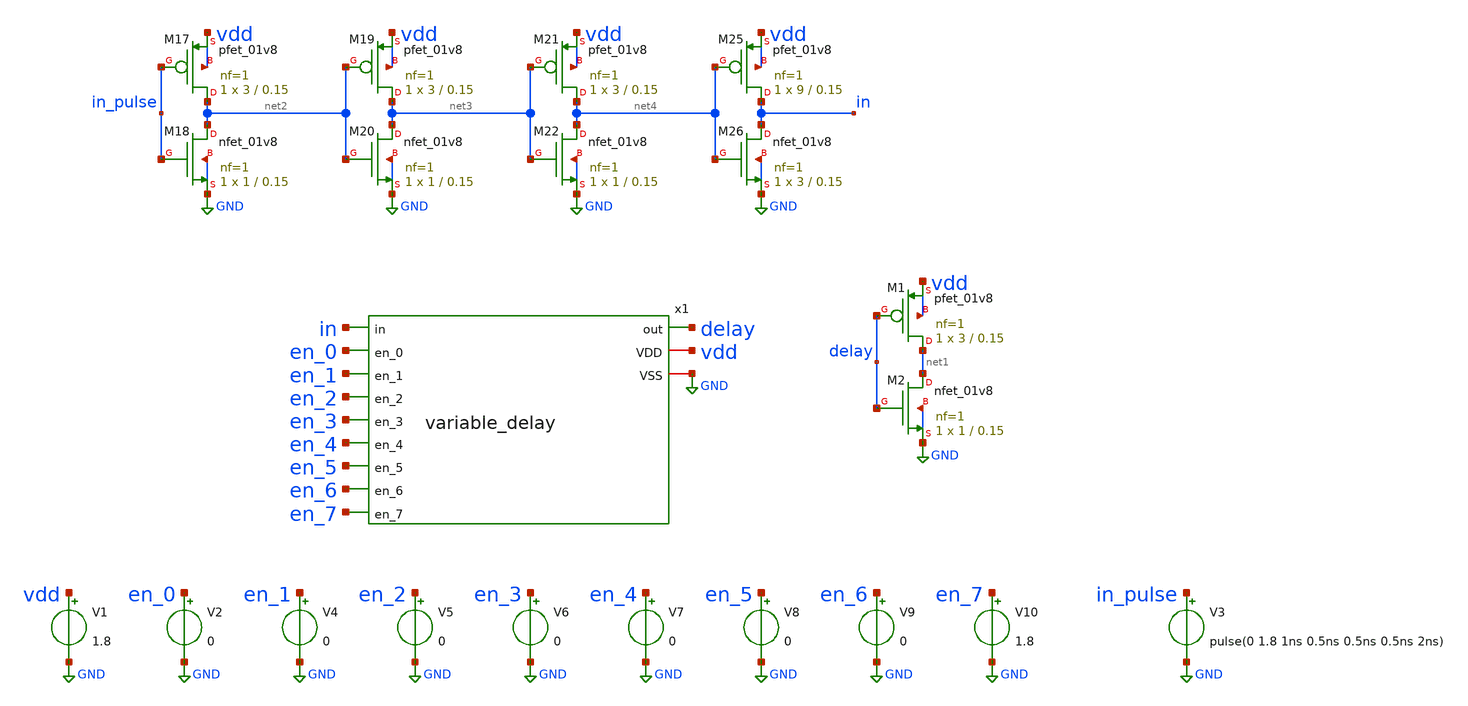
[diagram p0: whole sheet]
** sch_path: xschem/variable_delay_tb.sch
**.subckt variable_delay_tb
x1 in en_0 en_1 en_2 en_3 en_4 en_5 en_6 en_7 delay vdd GND variable_delay
V1 vdd GND 1.8
V3 in_pulse GND pulse(0 1.8 1ns 0.5ns 0.5ns 0.5ns 2ns)
XM1 net1 delay vdd vdd sky130_fd_pr__pfet_01v8 L=0.15 W=3 nf=1 ad='int((nf+1)/2) * W/nf * 0.29' as='int((nf+2)/2) * W/nf * 0.29'
+ pd='2*int((nf+1)/2) * (W/nf + 0.29)' ps='2*int((nf+2)/2) * (W/nf + 0.29)' nrd='0.29 / W' nrs='0.29 / W'
+ sa=0 sb=0 sd=0 mult=1 m=1
XM2 net1 delay GND GND sky130_fd_pr__nfet_01v8 L=0.15 W=1 nf=1 ad='int((nf+1)/2) * W/nf * 0.29' as='int((nf+2)/2) * W/nf * 0.29'
+ pd='2*int((nf+1)/2) * (W/nf + 0.29)' ps='2*int((nf+2)/2) * (W/nf + 0.29)' nrd='0.29 / W' nrs='0.29 / W'
+ sa=0 sb=0 sd=0 mult=1 m=1
V2 en_0 GND 0
V4 en_1 GND 0
V5 en_2 GND 0
V6 en_3 GND 0
V7 en_4 GND 0
V8 en_5 GND 0
V9 en_6 GND 0
V10 en_7 GND 1.8
XM17 net2 in_pulse vdd vdd sky130_fd_pr__pfet_01v8 L=0.15 W=3 nf=1 ad='int((nf+1)/2) * W/nf * 0.29' as='int((nf+2)/2) * W/nf * 0.29'
+ pd='2*int((nf+1)/2) * (W/nf + 0.29)' ps='2*int((nf+2)/2) * (W/nf + 0.29)' nrd='0.29 / W' nrs='0.29 / W'
+ sa=0 sb=0 sd=0 mult=1 m=1
XM18 net2 in_pulse GND GND sky130_fd_pr__nfet_01v8 L=0.15 W=1 nf=1 ad='int((nf+1)/2) * W/nf * 0.29' as='int((nf+2)/2) * W/nf * 0.29'
+ pd='2*int((nf+1)/2) * (W/nf + 0.29)' ps='2*int((nf+2)/2) * (W/nf + 0.29)' nrd='0.29 / W' nrs='0.29 / W'
+ sa=0 sb=0 sd=0 mult=1 m=1
XM19 net3 net2 vdd vdd sky130_fd_pr__pfet_01v8 L=0.15 W=3 nf=1 ad='int((nf+1)/2) * W/nf * 0.29' as='int((nf+2)/2) * W/nf * 0.29'
+ pd='2*int((nf+1)/2) * (W/nf + 0.29)' ps='2*int((nf+2)/2) * (W/nf + 0.29)' nrd='0.29 / W' nrs='0.29 / W'
+ sa=0 sb=0 sd=0 mult=1 m=1
XM20 net3 net2 GND GND sky130_fd_pr__nfet_01v8 L=0.15 W=1 nf=1 ad='int((nf+1)/2) * W/nf * 0.29' as='int((nf+2)/2) * W/nf * 0.29'
+ pd='2*int((nf+1)/2) * (W/nf + 0.29)' ps='2*int((nf+2)/2) * (W/nf + 0.29)' nrd='0.29 / W' nrs='0.29 / W'
+ sa=0 sb=0 sd=0 mult=1 m=1
XM21 net4 net3 vdd vdd sky130_fd_pr__pfet_01v8 L=0.15 W=3 nf=1 ad='int((nf+1)/2) * W/nf * 0.29' as='int((nf+2)/2) * W/nf * 0.29'
+ pd='2*int((nf+1)/2) * (W/nf + 0.29)' ps='2*int((nf+2)/2) * (W/nf + 0.29)' nrd='0.29 / W' nrs='0.29 / W'
+ sa=0 sb=0 sd=0 mult=1 m=1
XM22 net4 net3 GND GND sky130_fd_pr__nfet_01v8 L=0.15 W=1 nf=1 ad='int((nf+1)/2) * W/nf * 0.29' as='int((nf+2)/2) * W/nf * 0.29'
+ pd='2*int((nf+1)/2) * (W/nf + 0.29)' ps='2*int((nf+2)/2) * (W/nf + 0.29)' nrd='0.29 / W' nrs='0.29 / W'
+ sa=0 sb=0 sd=0 mult=1 m=1
XM25 in net4 vdd vdd sky130_fd_pr__pfet_01v8 L=0.15 W=9 nf=1 ad='int((nf+1)/2) * W/nf * 0.29' as='int((nf+2)/2) * W/nf * 0.29'
+ pd='2*int((nf+1)/2) * (W/nf + 0.29)' ps='2*int((nf+2)/2) * (W/nf + 0.29)' nrd='0.29 / W' nrs='0.29 / W'
+ sa=0 sb=0 sd=0 mult=1 m=1
XM26 in net4 GND GND sky130_fd_pr__nfet_01v8 L=0.15 W=3 nf=1 ad='int((nf+1)/2) * W/nf * 0.29' as='int((nf+2)/2) * W/nf * 0.29'
+ pd='2*int((nf+1)/2) * (W/nf + 0.29)' ps='2*int((nf+2)/2) * (W/nf + 0.29)' nrd='0.29 / W' nrs='0.29 / W'
+ sa=0 sb=0 sd=0 mult=1 m=1
**** begin user architecture code

** opencircuitdesign pdks install
.lib $::SKYWATER_MODELS/sky130.lib.spice tt





.tran 0.0001n 5n
.save v(in) v(delay)

.control
run
set wr_vecnames
wrdata variable_delay_7_tb.txt v(in) v(delay)
.endc


**** end user architecture code
**.ends

* expanding   symbol:  variable_delay.sym # of pins=12
** sym_path: xschem/variable_delay.sym
** sch_path: xschem/variable_delay.sch
.subckt variable_delay in en_0 en_1 en_2 en_3 en_4 en_5 en_6 en_7 out VDD VSS
*.iopin VDD
*.ipin in
*.opin out
*.iopin VSS
*.ipin en_0
*.ipin en_1
*.ipin en_2
*.ipin en_3
*.ipin en_4
*.ipin en_5
*.ipin en_6
*.ipin en_7
x1 in en_0 out_1 forward_0 out VDD VSS variable_delay_unit
x2 forward_0 en_1 out_2 forward_1 out_1 VDD VSS variable_delay_unit
x3 forward_1 en_2 out_3 forward_2 out_2 VDD VSS variable_delay_unit
x4 forward_2 en_3 out_4 forward_3 out_3 VDD VSS variable_delay_unit
x5 forward_3 en_4 out_5 forward_4 out_4 VDD VSS variable_delay_unit
x6 forward_4 en_5 out_6 forward_5 out_5 VDD VSS variable_delay_unit
x7 forward_5 en_6 out_7 forward_6 out_6 VDD VSS variable_delay_unit
x8 forward_6 en_7 out_8 forward_7 out_7 VDD VSS variable_delay_unit
x9 forward_7 VDD VSS net1 out_8 VDD VSS variable_delay_unit
.ends


* expanding   symbol:  variable_delay_unit.sym # of pins=7
** sym_path: xschem/variable_delay_unit.sym
** sch_path: xschem/variable_delay_unit.sch
.subckt variable_delay_unit in en back forward out VDD VSS
*.iopin VDD
*.ipin in
*.opin out
*.iopin VSS
*.ipin en
*.ipin back
*.opin forward
x1 forward en nen out VDD VSS tristate_inverter
x2 in forward VDD VSS inverter_2
x3 en nen VDD VSS inverter_2
x4 back nen en out VDD VSS tristate_inverter
.ends


* expanding   symbol:  tristate_inverter.sym # of pins=6
** sym_path: xschem/tristate_inverter.sym
** sch_path: xschem/tristate_inverter.sch
.subckt tristate_inverter in en nen out VDD VSS
*.iopin VDD
*.ipin in
*.opin out
*.iopin VSS
*.ipin en
*.ipin nen
XM5 out in net2 VDD sky130_fd_pr__pfet_01v8 L=0.15 W=3 nf=1 ad='int((nf+1)/2) * W/nf * 0.29' as='int((nf+2)/2) * W/nf * 0.29'
+ pd='2*int((nf+1)/2) * (W/nf + 0.29)' ps='2*int((nf+2)/2) * (W/nf + 0.29)' nrd='0.29 / W' nrs='0.29 / W'
+ sa=0 sb=0 sd=0 mult=1 m=1
XM7 out in net1 VSS sky130_fd_pr__nfet_01v8 L=0.15 W=1 nf=1 ad='int((nf+1)/2) * W/nf * 0.29' as='int((nf+2)/2) * W/nf * 0.29'
+ pd='2*int((nf+1)/2) * (W/nf + 0.29)' ps='2*int((nf+2)/2) * (W/nf + 0.29)' nrd='0.29 / W' nrs='0.29 / W'
+ sa=0 sb=0 sd=0 mult=1 m=1
XM1 net2 nen VDD VDD sky130_fd_pr__pfet_01v8 L=0.15 W=9 nf=1 ad='int((nf+1)/2) * W/nf * 0.29' as='int((nf+2)/2) * W/nf * 0.29'
+ pd='2*int((nf+1)/2) * (W/nf + 0.29)' ps='2*int((nf+2)/2) * (W/nf + 0.29)' nrd='0.29 / W' nrs='0.29 / W'
+ sa=0 sb=0 sd=0 mult=1 m=1
XM2 net1 en VSS VSS sky130_fd_pr__nfet_01v8 L=0.15 W=3 nf=1 ad='int((nf+1)/2) * W/nf * 0.29' as='int((nf+2)/2) * W/nf * 0.29'
+ pd='2*int((nf+1)/2) * (W/nf + 0.29)' ps='2*int((nf+2)/2) * (W/nf + 0.29)' nrd='0.29 / W' nrs='0.29 / W'
+ sa=0 sb=0 sd=0 mult=1 m=1
.ends


* expanding   symbol:  inverter_2.sym # of pins=4
** sym_path: xschem/inverter_2.sym
** sch_path: xschem/inverter_2.sch
.subckt inverter_2 in out VDD VSS
*.iopin VDD
*.ipin in
*.opin out
*.iopin VSS
XM1 out in VDD VDD sky130_fd_pr__pfet_01v8 L=0.15 W=3 nf=1 ad='int((nf+1)/2) * W/nf * 0.29' as='int((nf+2)/2) * W/nf * 0.29'
+ pd='2*int((nf+1)/2) * (W/nf + 0.29)' ps='2*int((nf+2)/2) * (W/nf + 0.29)' nrd='0.29 / W' nrs='0.29 / W'
+ sa=0 sb=0 sd=0 mult=1 m=1
XM2 out in VSS VSS sky130_fd_pr__nfet_01v8 L=0.15 W=1 nf=1 ad='int((nf+1)/2) * W/nf * 0.29' as='int((nf+2)/2) * W/nf * 0.29'
+ pd='2*int((nf+1)/2) * (W/nf + 0.29)' ps='2*int((nf+2)/2) * (W/nf + 0.29)' nrd='0.29 / W' nrs='0.29 / W'
+ sa=0 sb=0 sd=0 mult=1 m=1
.ends

.GLOBAL GND
.end
